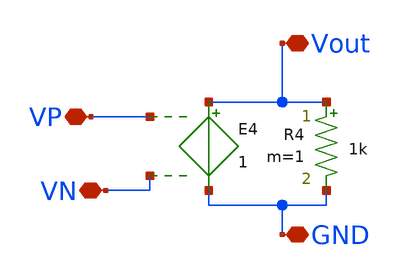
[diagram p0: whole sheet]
** sch_path: SAR_ADC/xschem/spice/symbols/Vdiffmeter.sch
**.subckt Vdiffmeter Vout GND VP VN
*.iopin Vout
*.iopin GND
*.iopin VP
*.iopin VN
R4 Vout GND 1k m=1
E4 Vout GND VP VN 1
**.ends
.end
